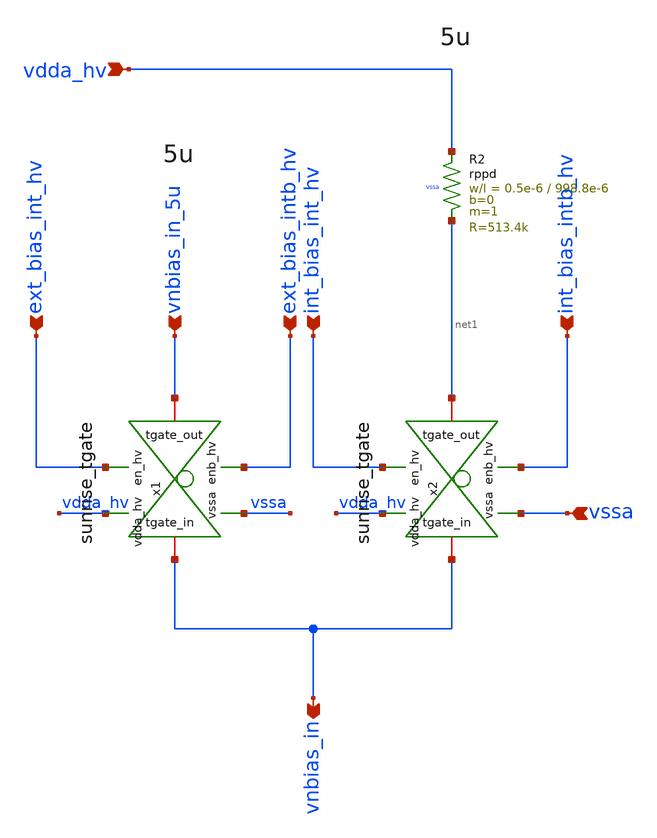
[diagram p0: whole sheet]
** sch_path: Schematics_Layout/sunrise_int_ext_bias/sunrise_int_ext_bias.sch
**.subckt sunrise_int_ext_bias vnbias_in_5u vdda_hv ext_bias_intb_hv ext_bias_int_hv
*+ int_bias_intb_hv int_bias_int_hv vssa vnbias_in
*.ipin vnbias_in_5u
*.ipin vdda_hv
*.ipin ext_bias_intb_hv
*.ipin ext_bias_int_hv
*.ipin int_bias_intb_hv
*.ipin int_bias_int_hv
*.ipin vssa
*.opin vnbias_in
XR2 vdda_hv net1 vssa rppd w=0.5e-6 l=998.8e-6 m=1 b=0 mm_ok=1
x1 vdda_hv vssa ext_bias_int_hv vnbias_in vnbias_in_5u ext_bias_intb_hv sunrise_tgate
x2 vdda_hv vssa int_bias_int_hv vnbias_in net1 int_bias_intb_hv sunrise_tgate
**.ends
.end
